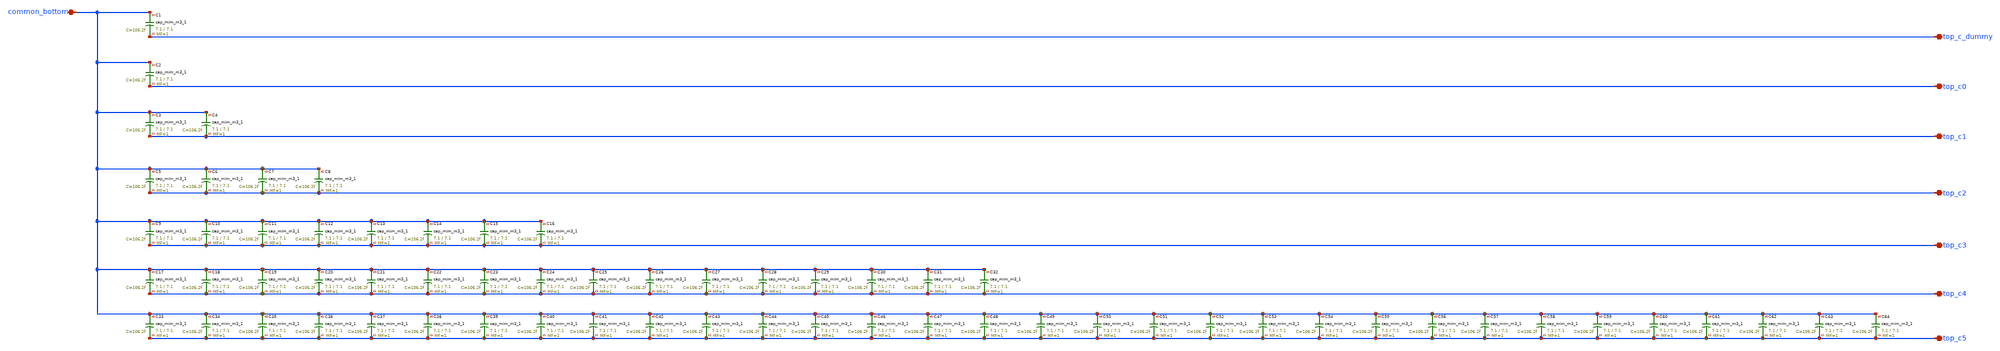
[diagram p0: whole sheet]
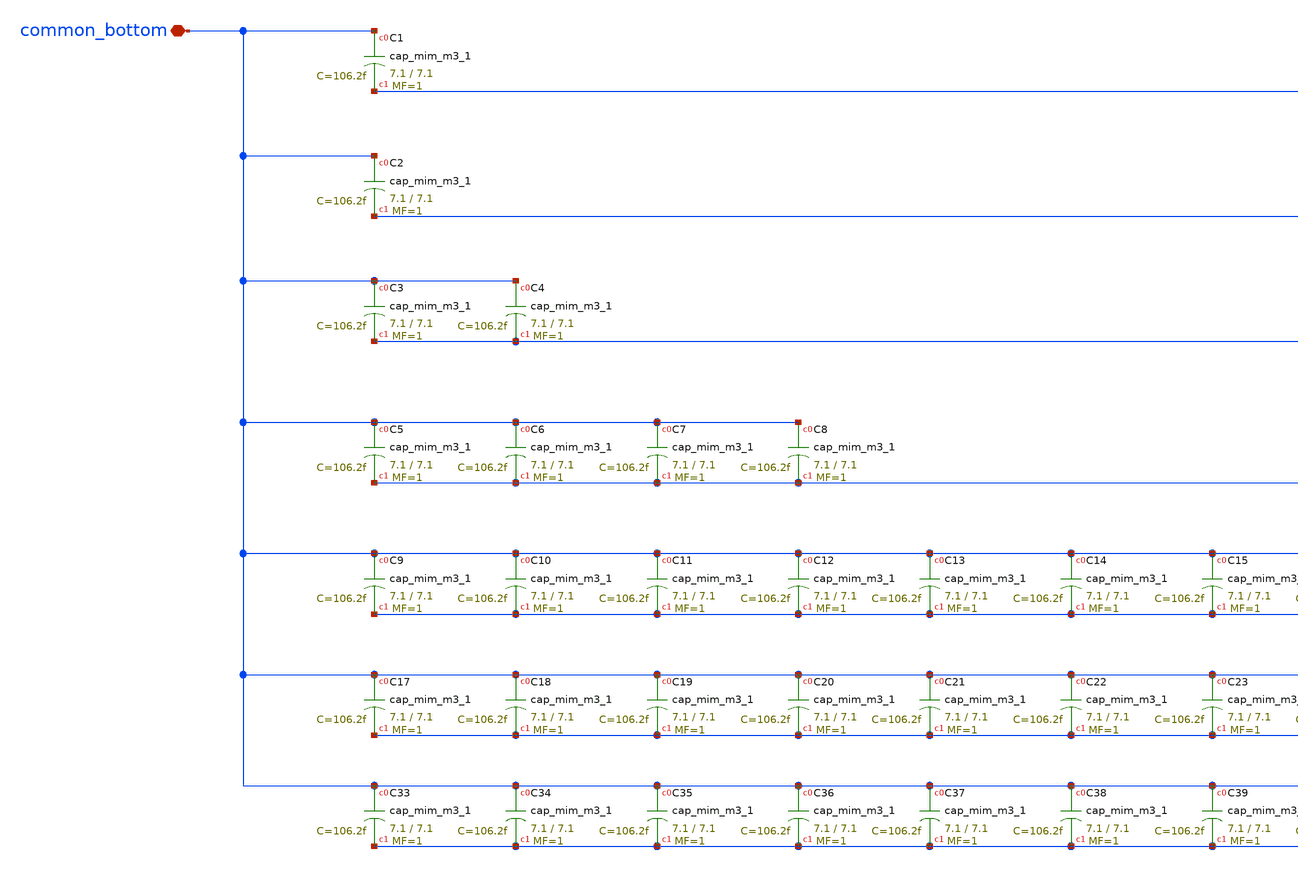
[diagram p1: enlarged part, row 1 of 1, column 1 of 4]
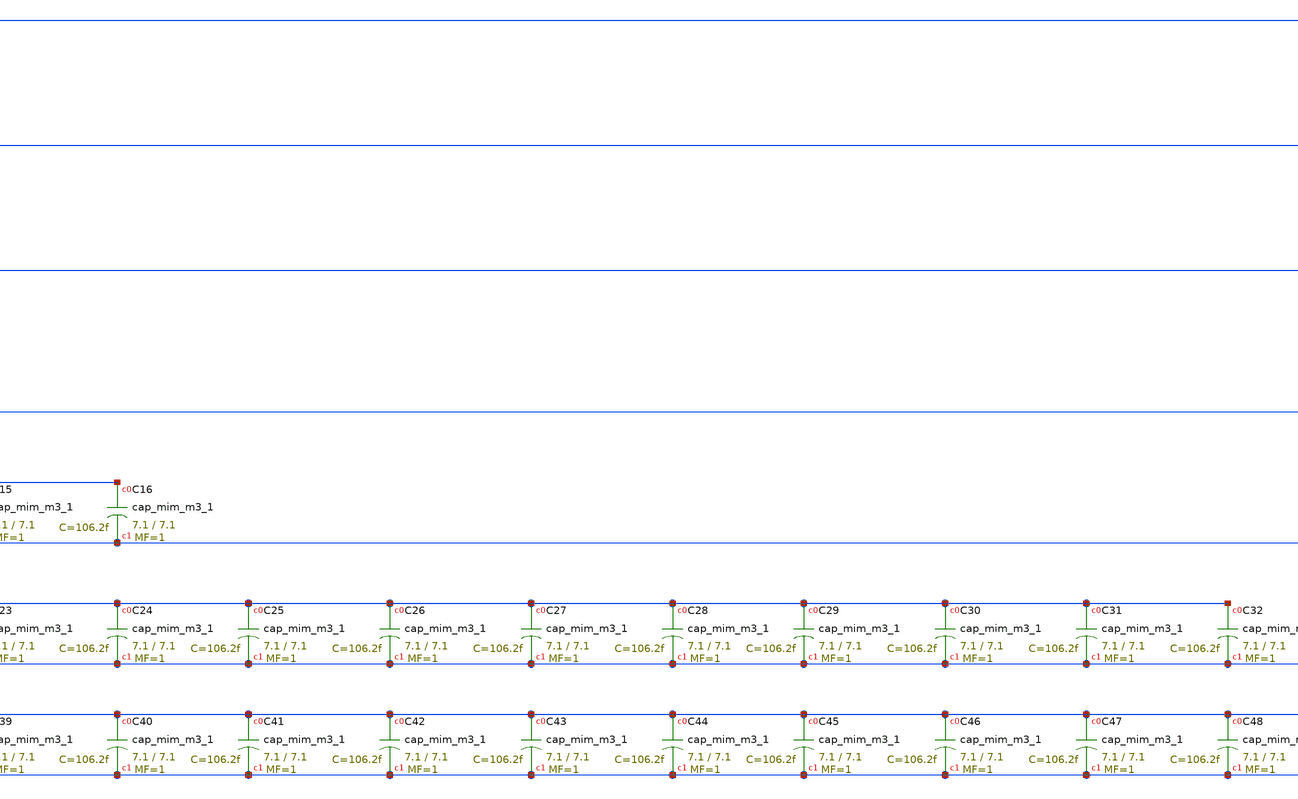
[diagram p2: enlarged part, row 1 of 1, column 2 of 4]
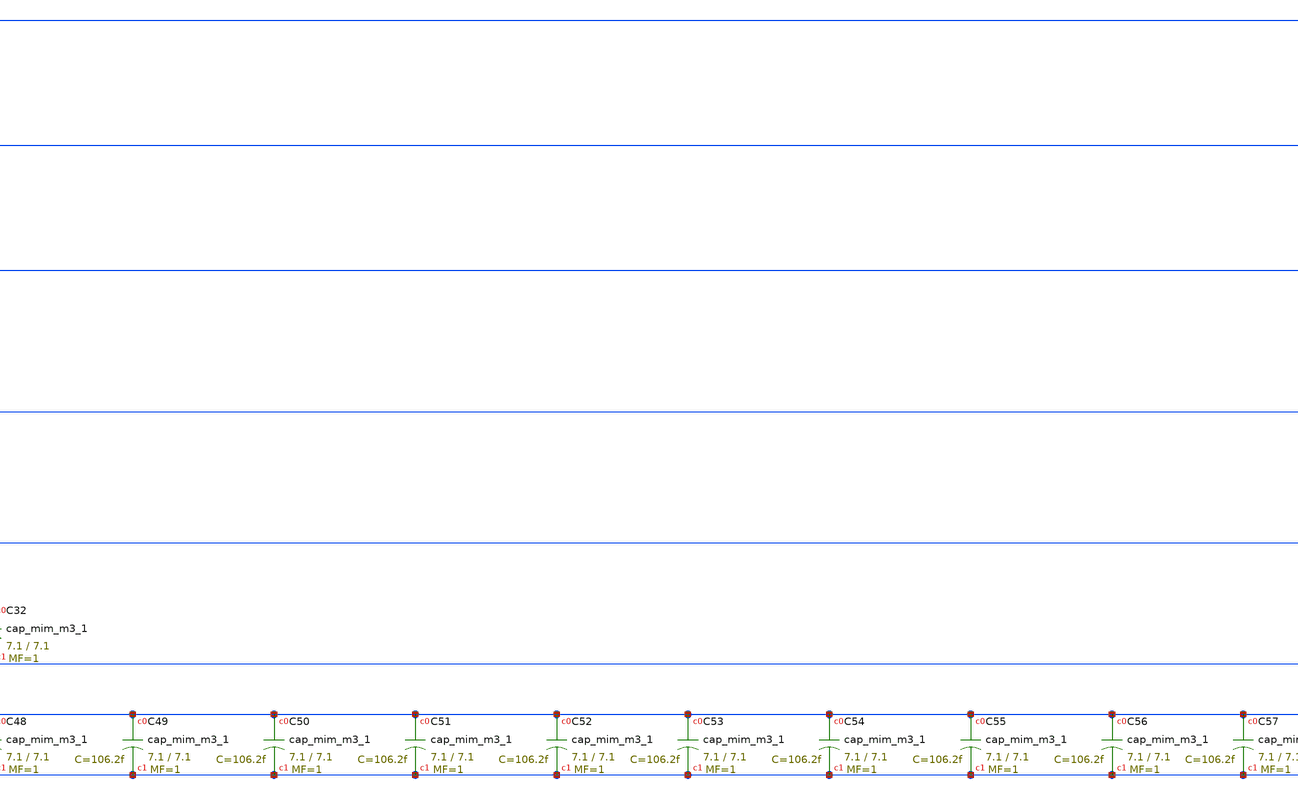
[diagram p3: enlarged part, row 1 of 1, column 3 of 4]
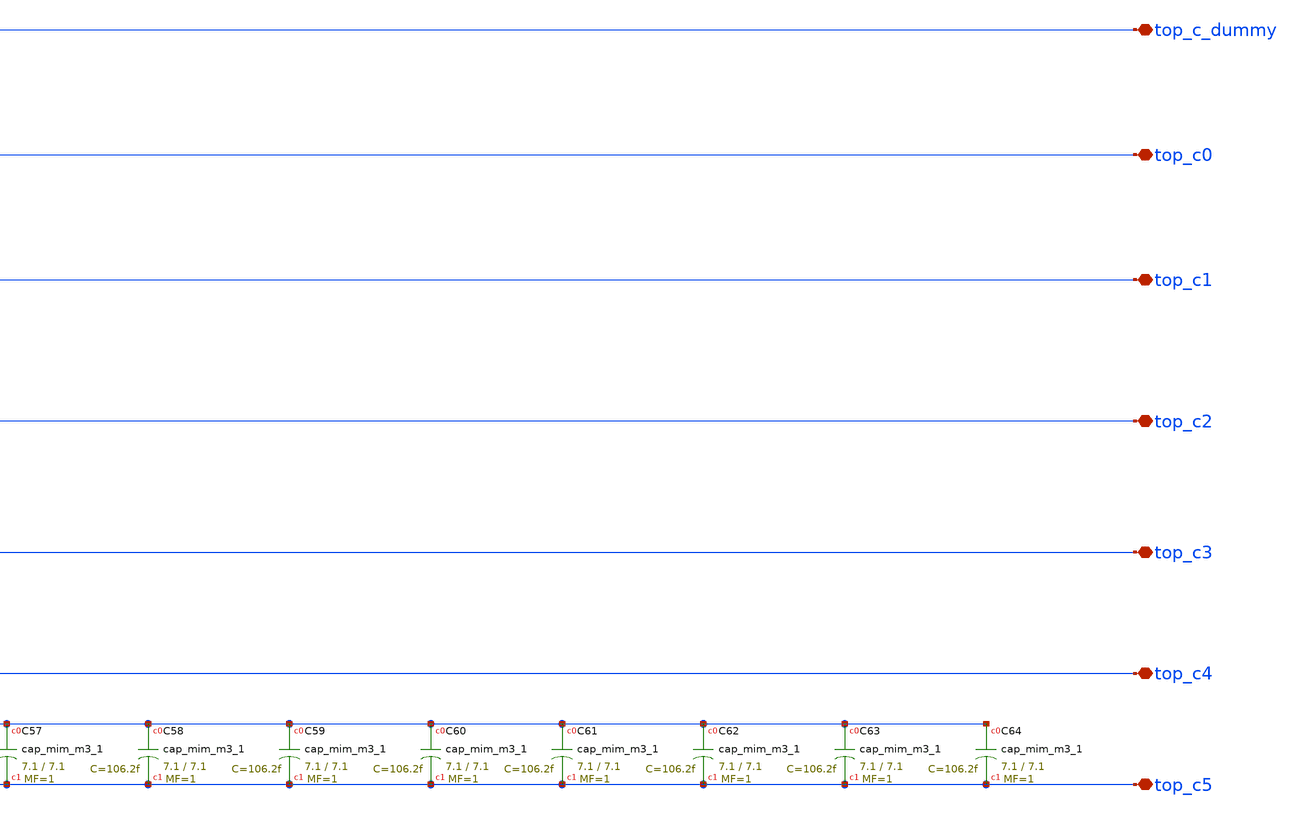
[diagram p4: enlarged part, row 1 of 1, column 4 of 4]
** sch_path: SKY130/SAR-ADC/SAR-ADC_1.8V/cap_array.sch
**.subckt cap_array common_bottom top_c_dummy top_c0 top_c5 top_c4 top_c3 top_c2 top_c1
*.iopin common_bottom
*.iopin top_c_dummy
*.iopin top_c0
*.iopin top_c5
*.iopin top_c4
*.iopin top_c3
*.iopin top_c2
*.iopin top_c1
XC1 common_bottom top_c_dummy sky130_fd_pr__cap_mim_m3_1 W=7.1 L=7.1 MF=1 m=1
XC2 common_bottom top_c0 sky130_fd_pr__cap_mim_m3_1 W=7.1 L=7.1 MF=1 m=1
XC3 common_bottom top_c1 sky130_fd_pr__cap_mim_m3_1 W=7.1 L=7.1 MF=1 m=1
XC4 common_bottom top_c1 sky130_fd_pr__cap_mim_m3_1 W=7.1 L=7.1 MF=1 m=1
XC5 common_bottom top_c2 sky130_fd_pr__cap_mim_m3_1 W=7.1 L=7.1 MF=1 m=1
XC6 common_bottom top_c2 sky130_fd_pr__cap_mim_m3_1 W=7.1 L=7.1 MF=1 m=1
XC7 common_bottom top_c2 sky130_fd_pr__cap_mim_m3_1 W=7.1 L=7.1 MF=1 m=1
XC8 common_bottom top_c2 sky130_fd_pr__cap_mim_m3_1 W=7.1 L=7.1 MF=1 m=1
XC9 common_bottom top_c3 sky130_fd_pr__cap_mim_m3_1 W=7.1 L=7.1 MF=1 m=1
XC10 common_bottom top_c3 sky130_fd_pr__cap_mim_m3_1 W=7.1 L=7.1 MF=1 m=1
XC11 common_bottom top_c3 sky130_fd_pr__cap_mim_m3_1 W=7.1 L=7.1 MF=1 m=1
XC12 common_bottom top_c3 sky130_fd_pr__cap_mim_m3_1 W=7.1 L=7.1 MF=1 m=1
XC13 common_bottom top_c3 sky130_fd_pr__cap_mim_m3_1 W=7.1 L=7.1 MF=1 m=1
XC14 common_bottom top_c3 sky130_fd_pr__cap_mim_m3_1 W=7.1 L=7.1 MF=1 m=1
XC15 common_bottom top_c3 sky130_fd_pr__cap_mim_m3_1 W=7.1 L=7.1 MF=1 m=1
XC16 common_bottom top_c3 sky130_fd_pr__cap_mim_m3_1 W=7.1 L=7.1 MF=1 m=1
XC17 common_bottom top_c4 sky130_fd_pr__cap_mim_m3_1 W=7.1 L=7.1 MF=1 m=1
XC18 common_bottom top_c4 sky130_fd_pr__cap_mim_m3_1 W=7.1 L=7.1 MF=1 m=1
XC19 common_bottom top_c4 sky130_fd_pr__cap_mim_m3_1 W=7.1 L=7.1 MF=1 m=1
XC20 common_bottom top_c4 sky130_fd_pr__cap_mim_m3_1 W=7.1 L=7.1 MF=1 m=1
XC21 common_bottom top_c4 sky130_fd_pr__cap_mim_m3_1 W=7.1 L=7.1 MF=1 m=1
XC22 common_bottom top_c4 sky130_fd_pr__cap_mim_m3_1 W=7.1 L=7.1 MF=1 m=1
XC23 common_bottom top_c4 sky130_fd_pr__cap_mim_m3_1 W=7.1 L=7.1 MF=1 m=1
XC24 common_bottom top_c4 sky130_fd_pr__cap_mim_m3_1 W=7.1 L=7.1 MF=1 m=1
XC25 common_bottom top_c4 sky130_fd_pr__cap_mim_m3_1 W=7.1 L=7.1 MF=1 m=1
XC26 common_bottom top_c4 sky130_fd_pr__cap_mim_m3_1 W=7.1 L=7.1 MF=1 m=1
XC27 common_bottom top_c4 sky130_fd_pr__cap_mim_m3_1 W=7.1 L=7.1 MF=1 m=1
XC28 common_bottom top_c4 sky130_fd_pr__cap_mim_m3_1 W=7.1 L=7.1 MF=1 m=1
XC29 common_bottom top_c4 sky130_fd_pr__cap_mim_m3_1 W=7.1 L=7.1 MF=1 m=1
XC30 common_bottom top_c4 sky130_fd_pr__cap_mim_m3_1 W=7.1 L=7.1 MF=1 m=1
XC31 common_bottom top_c4 sky130_fd_pr__cap_mim_m3_1 W=7.1 L=7.1 MF=1 m=1
XC32 common_bottom top_c4 sky130_fd_pr__cap_mim_m3_1 W=7.1 L=7.1 MF=1 m=1
XC33 common_bottom top_c5 sky130_fd_pr__cap_mim_m3_1 W=7.1 L=7.1 MF=1 m=1
XC34 common_bottom top_c5 sky130_fd_pr__cap_mim_m3_1 W=7.1 L=7.1 MF=1 m=1
XC35 common_bottom top_c5 sky130_fd_pr__cap_mim_m3_1 W=7.1 L=7.1 MF=1 m=1
XC36 common_bottom top_c5 sky130_fd_pr__cap_mim_m3_1 W=7.1 L=7.1 MF=1 m=1
XC37 common_bottom top_c5 sky130_fd_pr__cap_mim_m3_1 W=7.1 L=7.1 MF=1 m=1
XC38 common_bottom top_c5 sky130_fd_pr__cap_mim_m3_1 W=7.1 L=7.1 MF=1 m=1
XC39 common_bottom top_c5 sky130_fd_pr__cap_mim_m3_1 W=7.1 L=7.1 MF=1 m=1
XC40 common_bottom top_c5 sky130_fd_pr__cap_mim_m3_1 W=7.1 L=7.1 MF=1 m=1
XC41 common_bottom top_c5 sky130_fd_pr__cap_mim_m3_1 W=7.1 L=7.1 MF=1 m=1
XC42 common_bottom top_c5 sky130_fd_pr__cap_mim_m3_1 W=7.1 L=7.1 MF=1 m=1
XC43 common_bottom top_c5 sky130_fd_pr__cap_mim_m3_1 W=7.1 L=7.1 MF=1 m=1
XC44 common_bottom top_c5 sky130_fd_pr__cap_mim_m3_1 W=7.1 L=7.1 MF=1 m=1
XC45 common_bottom top_c5 sky130_fd_pr__cap_mim_m3_1 W=7.1 L=7.1 MF=1 m=1
XC46 common_bottom top_c5 sky130_fd_pr__cap_mim_m3_1 W=7.1 L=7.1 MF=1 m=1
XC47 common_bottom top_c5 sky130_fd_pr__cap_mim_m3_1 W=7.1 L=7.1 MF=1 m=1
XC48 common_bottom top_c5 sky130_fd_pr__cap_mim_m3_1 W=7.1 L=7.1 MF=1 m=1
XC49 common_bottom top_c5 sky130_fd_pr__cap_mim_m3_1 W=7.1 L=7.1 MF=1 m=1
XC50 common_bottom top_c5 sky130_fd_pr__cap_mim_m3_1 W=7.1 L=7.1 MF=1 m=1
XC51 common_bottom top_c5 sky130_fd_pr__cap_mim_m3_1 W=7.1 L=7.1 MF=1 m=1
XC52 common_bottom top_c5 sky130_fd_pr__cap_mim_m3_1 W=7.1 L=7.1 MF=1 m=1
XC53 common_bottom top_c5 sky130_fd_pr__cap_mim_m3_1 W=7.1 L=7.1 MF=1 m=1
XC54 common_bottom top_c5 sky130_fd_pr__cap_mim_m3_1 W=7.1 L=7.1 MF=1 m=1
XC55 common_bottom top_c5 sky130_fd_pr__cap_mim_m3_1 W=7.1 L=7.1 MF=1 m=1
XC56 common_bottom top_c5 sky130_fd_pr__cap_mim_m3_1 W=7.1 L=7.1 MF=1 m=1
XC57 common_bottom top_c5 sky130_fd_pr__cap_mim_m3_1 W=7.1 L=7.1 MF=1 m=1
XC58 common_bottom top_c5 sky130_fd_pr__cap_mim_m3_1 W=7.1 L=7.1 MF=1 m=1
XC59 common_bottom top_c5 sky130_fd_pr__cap_mim_m3_1 W=7.1 L=7.1 MF=1 m=1
XC60 common_bottom top_c5 sky130_fd_pr__cap_mim_m3_1 W=7.1 L=7.1 MF=1 m=1
XC61 common_bottom top_c5 sky130_fd_pr__cap_mim_m3_1 W=7.1 L=7.1 MF=1 m=1
XC62 common_bottom top_c5 sky130_fd_pr__cap_mim_m3_1 W=7.1 L=7.1 MF=1 m=1
XC63 common_bottom top_c5 sky130_fd_pr__cap_mim_m3_1 W=7.1 L=7.1 MF=1 m=1
XC64 common_bottom top_c5 sky130_fd_pr__cap_mim_m3_1 W=7.1 L=7.1 MF=1 m=1
**.ends
.end
